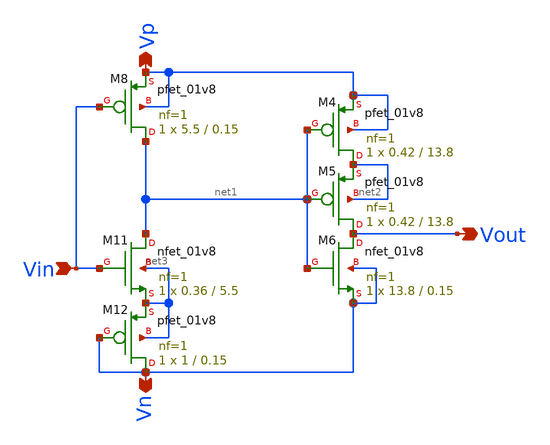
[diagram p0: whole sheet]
** sch_path: xschem/Vth_sch/Symbol/th13.sch
**.subckt th13 Vn Vp Vin Vout
*.opin Vn
*.opin Vp
*.ipin Vin
*.opin Vout
XM4 net2 net1 Vp Vp sky130_fd_pr__pfet_01v8 L=13.8 W=0.42 nf=1 ad='int((nf+1)/2) * W/nf * 0.29' as='int((nf+2)/2) * W/nf * 0.29'
+ pd='2*int((nf+1)/2) * (W/nf + 0.29)' ps='2*int((nf+2)/2) * (W/nf + 0.29)' nrd='0.29 / W' nrs='0.29 / W'
+ sa=0 sb=0 sd=0 mult=1 m=1
XM5 Vout net1 net2 net2 sky130_fd_pr__pfet_01v8 L=13.8 W=0.42 nf=1 ad='int((nf+1)/2) * W/nf * 0.29' as='int((nf+2)/2) * W/nf * 0.29'
+ pd='2*int((nf+1)/2) * (W/nf + 0.29)' ps='2*int((nf+2)/2) * (W/nf + 0.29)' nrd='0.29 / W' nrs='0.29 / W'
+ sa=0 sb=0 sd=0 mult=1 m=1
XM6 Vout net1 Vn Vn sky130_fd_pr__nfet_01v8 L=0.15 W=13.8 nf=1 ad='int((nf+1)/2) * W/nf * 0.29' as='int((nf+2)/2) * W/nf * 0.29'
+ pd='2*int((nf+1)/2) * (W/nf + 0.29)' ps='2*int((nf+2)/2) * (W/nf + 0.29)' nrd='0.29 / W' nrs='0.29 / W'
+ sa=0 sb=0 sd=0 mult=1 m=1
XM8 net1 Vin Vp Vp sky130_fd_pr__pfet_01v8 L=0.15 W=5.5 nf=1 ad='int((nf+1)/2) * W/nf * 0.29' as='int((nf+2)/2) * W/nf * 0.29'
+ pd='2*int((nf+1)/2) * (W/nf + 0.29)' ps='2*int((nf+2)/2) * (W/nf + 0.29)' nrd='0.29 / W' nrs='0.29 / W'
+ sa=0 sb=0 sd=0 mult=1 m=1
XM11 net1 Vin net3 net3 sky130_fd_pr__nfet_01v8 L=5.5 W=0.36 nf=1 ad='int((nf+1)/2) * W/nf * 0.29' as='int((nf+2)/2) * W/nf * 0.29'
+ pd='2*int((nf+1)/2) * (W/nf + 0.29)' ps='2*int((nf+2)/2) * (W/nf + 0.29)' nrd='0.29 / W' nrs='0.29 / W'
+ sa=0 sb=0 sd=0 mult=1 m=1
XM12 Vn Vn net3 net3 sky130_fd_pr__pfet_01v8 L=0.15 W=1 nf=1 ad='int((nf+1)/2) * W/nf * 0.29' as='int((nf+2)/2) * W/nf * 0.29'
+ pd='2*int((nf+1)/2) * (W/nf + 0.29)' ps='2*int((nf+2)/2) * (W/nf + 0.29)' nrd='0.29 / W' nrs='0.29 / W'
+ sa=0 sb=0 sd=0 mult=1 m=1
**.ends
.end
